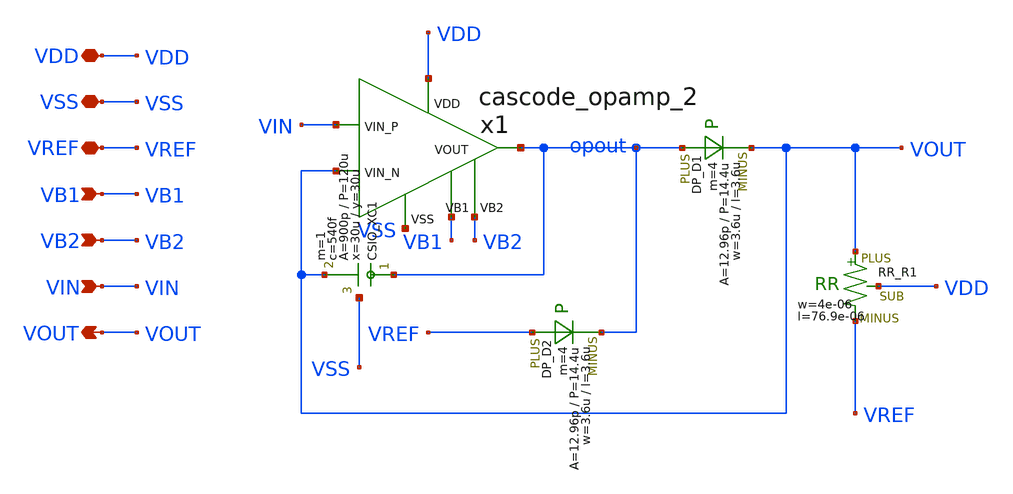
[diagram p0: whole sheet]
** sch_path: member_project/AM_Radio/noritsuna/xschem/ideal_diode.sch
**.subckt ideal_diode VDD VIN VOUT VSS VREF VB1 VB2
*.iopin VDD
*.ipin VIN
*.opin VOUT
*.iopin VSS
*.iopin VREF
*.ipin VB1
*.ipin VB2
XR1 VOUT VREF VDD F_RR w=4e-06 R=20k l=76.9e-06 tc1=0 tc2=0
x1 VDD VSS VIN VOUT opout VB2 VB1 cascode_opamp_2
XXC1 opout VOUT VSS F_CSIO c=540f x=30u y=30u m=1
DD1 opout VOUT DP m=4
DD2 VREF opout DP m=4
**.ends

* expanding   symbol:  cascode_opamp_2.sym # of pins=7
** sym_path: member_project/AM_Radio/noritsuna/xschem/cascode_opamp_2.sym
** sch_path: member_project/AM_Radio/noritsuna/xschem/cascode_opamp_2.sch
.subckt cascode_opamp_2 VDD VSS VIN_P VIN_N VOUT VB2 VB1
*.opin VOUT
*.ipin VIN_N
*.ipin VIN_P
*.ipin VSS
*.ipin VDD
*.ipin VB1
*.ipin VB2
MM2 net2 net1 VDD VDD PMOS w=240u l=8u as=0 ad=0 ps=0 pd=0 nrd=0 nrs=0 m=1
MM4 OUT1 VB2 MN_MDMY4 VSS NMOS w=84u l=8u as=0 ad=0 ps=0 pd=0 nrd=0 nrs=0 m=1
MM7 VOUT iB VDD VDD PMOS w=2400u l=8u as=0 ad=0 ps=0 pd=0 nrd=0 nrs=0 m=1
MM8 VOUT OUT1 VSS VSS NMOS w=1680u l=8u as=0 ad=0 ps=0 pd=0 nrd=0 nrs=0 m=1
MM16 net1 net1 VDD VDD PMOS w=240u l=8u as=0 ad=0 ps=0 pd=0 nrd=0 nrs=0 m=1
MM17 OUT1 MPN_MDMY3 net2 VDD PMOS w=240u l=8u as=0 ad=0 ps=0 pd=0 nrd=0 nrs=0 m=1
MM18 MPN_MDMY3 MPN_MDMY3 net1 VDD PMOS w=240u l=8u as=0 ad=0 ps=0 pd=0 nrd=0 nrs=0 m=1
MM19 MPN_MDMY3 VB2 MN_MDMY2 VSS NMOS w=84u l=8u as=0 ad=0 ps=0 pd=0 nrd=0 nrs=0 m=1
MM20 MN_MDMY4 VIN_P MN_MDMY5 VSS NMOS w=672u l=8u as=0 ad=0 ps=0 pd=0 nrd=0 nrs=0 m=1
MM21 MN_MDMY2 VIN_N MN_MDMY5 VSS NMOS w=672u l=8u as=0 ad=0 ps=0 pd=0 nrd=0 nrs=0 m=1
MM22 MN_MDMY5 VB1 VSS VSS NMOS w=84u l=8u as=0 ad=0 ps=0 pd=0 nrd=0 nrs=0 m=1
MM3 net3 net7 OUT1 VSS NMOS w=168u l=8u as=0 ad=0 ps=0 pd=0 nrd=0 nrs=0 m=1
MM6 net4 net4 VSS VSS NMOS w=168u l=8u as=0 ad=0 ps=0 pd=0 nrd=0 nrs=0 m=1
MM13 VB2 VB2 VB1 VSS NMOS w=84u l=8u as=0 ad=0 ps=0 pd=0 nrd=0 nrs=0 m=1
MM14 VB1 VB1 VSS VSS NMOS w=84u l=8u as=0 ad=0 ps=0 pd=0 nrd=0 nrs=0 m=1
MM23 VB4 VB4 VDD VDD PMOS w=240u l=8u as=0 ad=0 ps=0 pd=0 nrd=0 nrs=0 m=1
MM24 VB2 iB net5 VDD PMOS w=240u l=8u as=0 ad=0 ps=0 pd=0 nrd=0 nrs=0 m=1
MM25 net5 VB4 VDD VDD PMOS w=240u l=8u as=0 ad=0 ps=0 pd=0 nrd=0 nrs=0 m=1
MM26 iB iB VB4 VDD PMOS w=240u l=8u as=0 ad=0 ps=0 pd=0 nrd=0 nrs=0 m=1
MM1 net7 iB net6 VDD PMOS w=240u l=8u as=0 ad=0 ps=0 pd=0 nrd=0 nrs=0 m=1
MM9 net6 VB4 VDD VDD PMOS w=240u l=8u as=0 ad=0 ps=0 pd=0 nrd=0 nrs=0 m=1
MM5 net7 net7 net4 VSS NMOS w=168u l=8u as=0 ad=0 ps=0 pd=0 nrd=0 nrs=0 m=1
XXC1 net3 VOUT VSS F_CSIO c=540f x=30u y=30u m=1
XMDMYN2 MN_MDMY2 VSS VSS VSS NMOS w=42u l=8u as=0 ad=0 ps=0 pd=0 nrd=0 nrs=0 m=2
XMDMYN3 MPN_MDMY3 VSS VSS VSS NMOS w=7u l=8u as=0 ad=0 ps=0 pd=0 nrd=0 nrs=0 m=4
XMDMYN4 MN_MDMY4 VSS VSS VSS NMOS w=42u l=8u as=0 ad=0 ps=0 pd=0 nrd=0 nrs=0 m=2
XMDMYN5 MN_MDMY5 VSS VSS VSS NMOS w=42u l=8u as=0 ad=0 ps=0 pd=0 nrd=0 nrs=0 m=2
XMDMYN6 OUT1 VSS VSS VSS NMOS w=42u l=8u as=0 ad=0 ps=0 pd=0 nrd=0 nrs=0 m=4
XMDMYP1 iB VDD VDD VDD PMOS w=20u l=8u as=0 ad=0 ps=0 pd=0 nrd=0 nrs=0 m=4
XMDMYP2 MPN_MDMY3 VDD VDD VDD PMOS w=20u l=8u as=0 ad=0 ps=0 pd=0 nrd=0 nrs=0 m=4
XMDMYP3 VDD VDD VDD VDD PMOS w=60u l=8u as=0 ad=0 ps=0 pd=0 nrd=0 nrs=0 m=4
MM10 iB VB2 net8 VSS NMOS w=84u l=8u as=0 ad=0 ps=0 pd=0 nrd=0 nrs=0 m=1
MM11 net8 VB1 VSS VSS NMOS w=84u l=8u as=0 ad=0 ps=0 pd=0 nrd=0 nrs=0 m=1
XMDMYN7 iB VSS VSS VSS NMOS w=7u l=8u as=0 ad=0 ps=0 pd=0 nrd=0 nrs=0 m=4
.ends

.end
